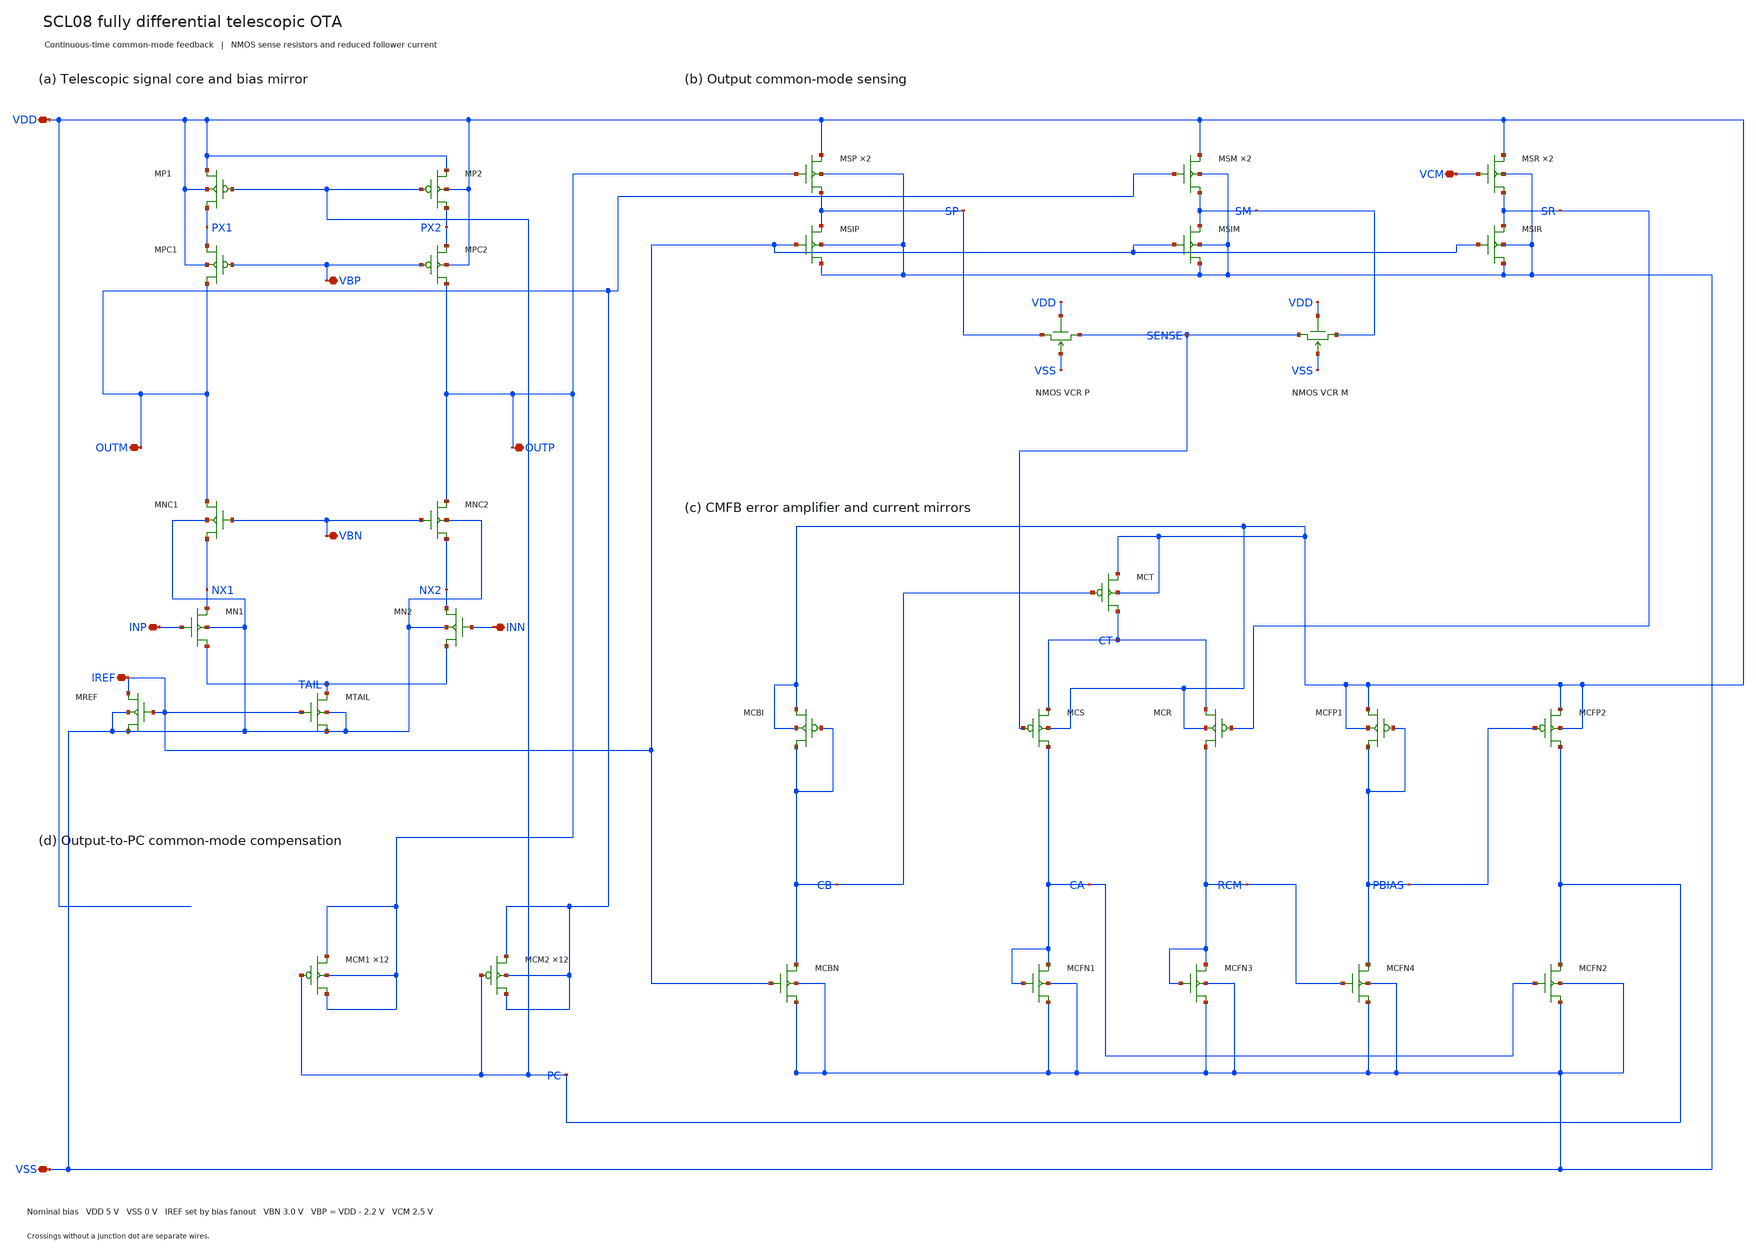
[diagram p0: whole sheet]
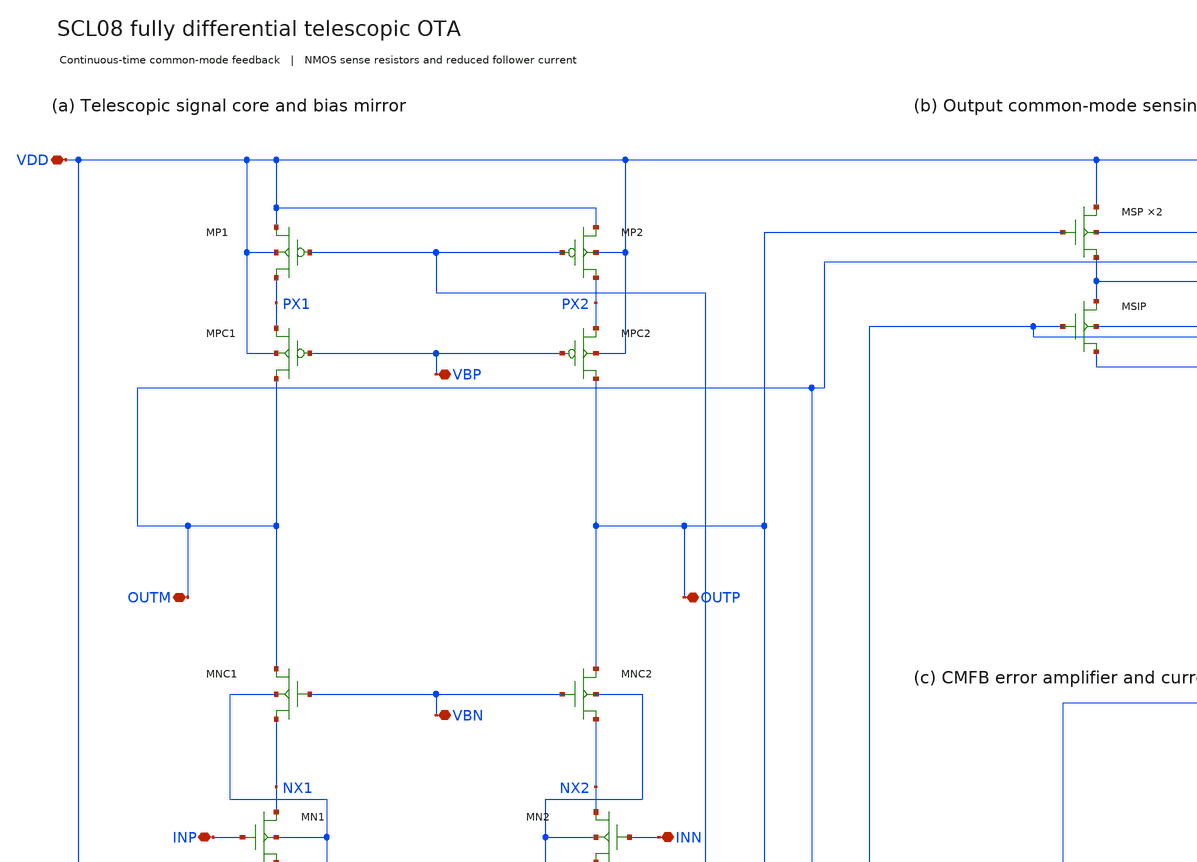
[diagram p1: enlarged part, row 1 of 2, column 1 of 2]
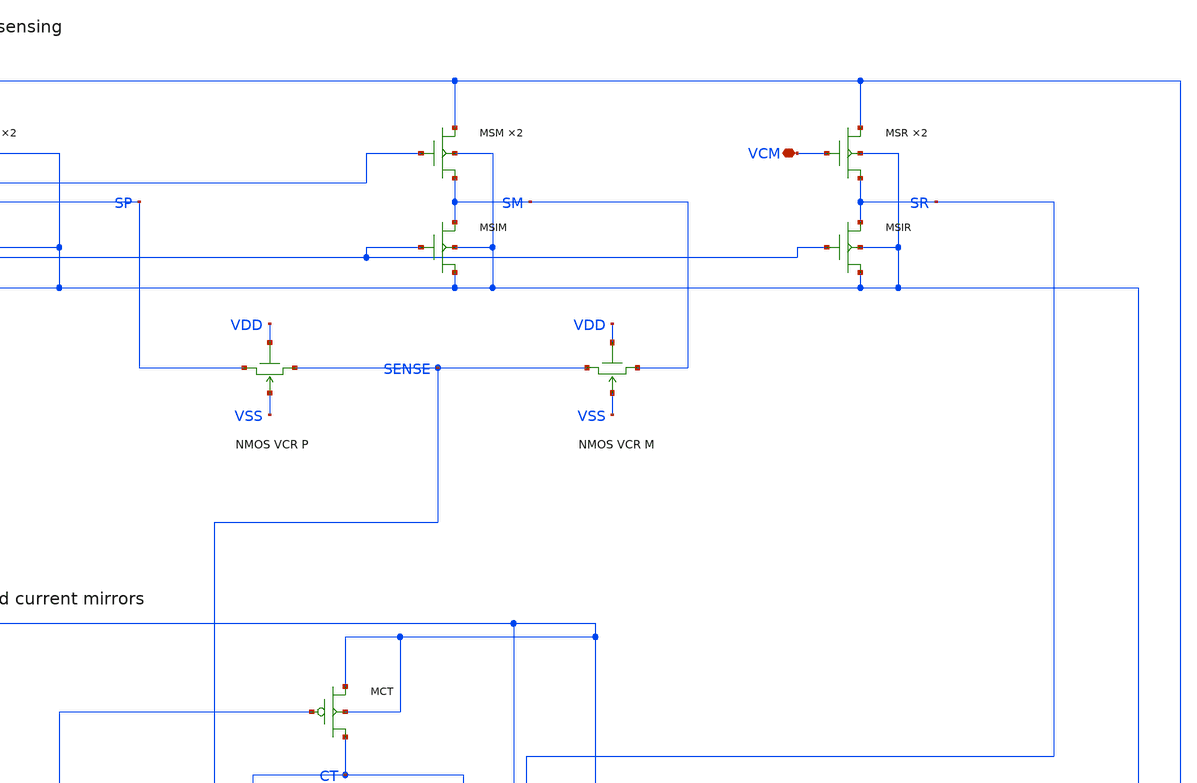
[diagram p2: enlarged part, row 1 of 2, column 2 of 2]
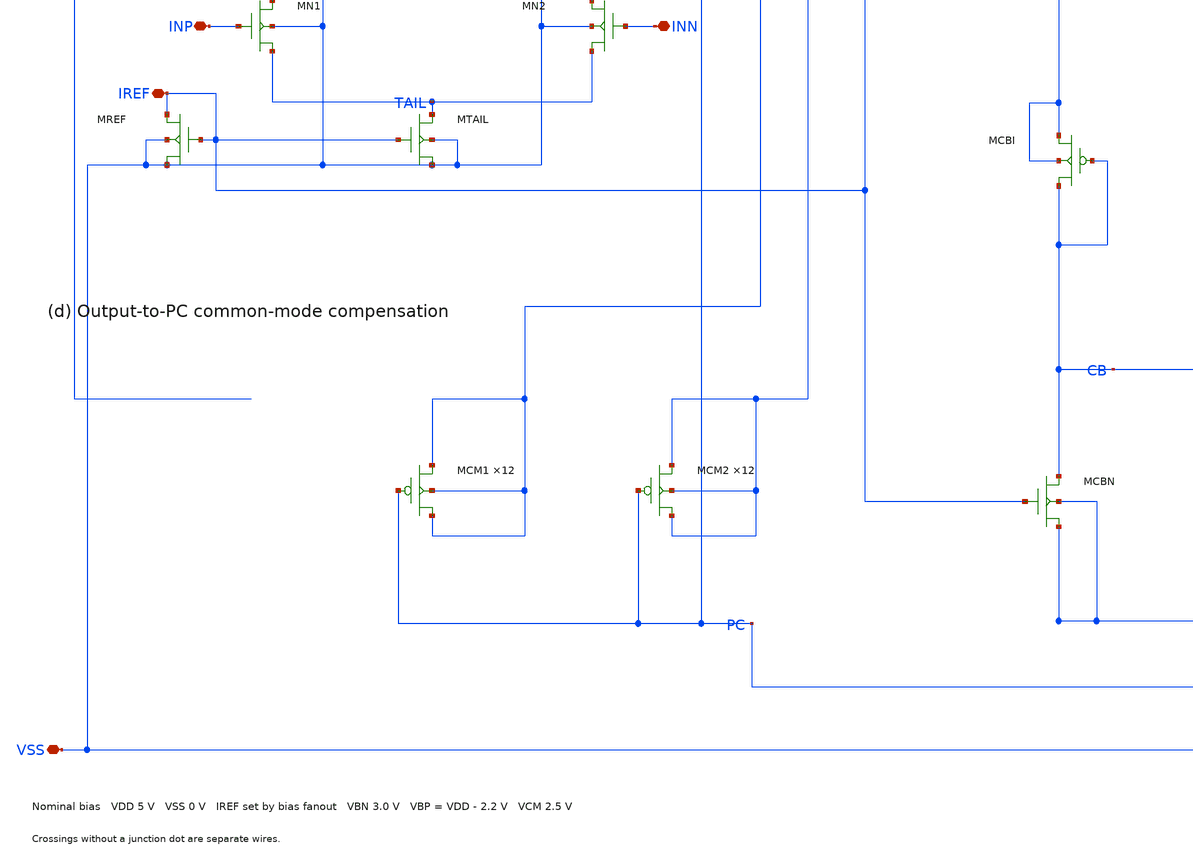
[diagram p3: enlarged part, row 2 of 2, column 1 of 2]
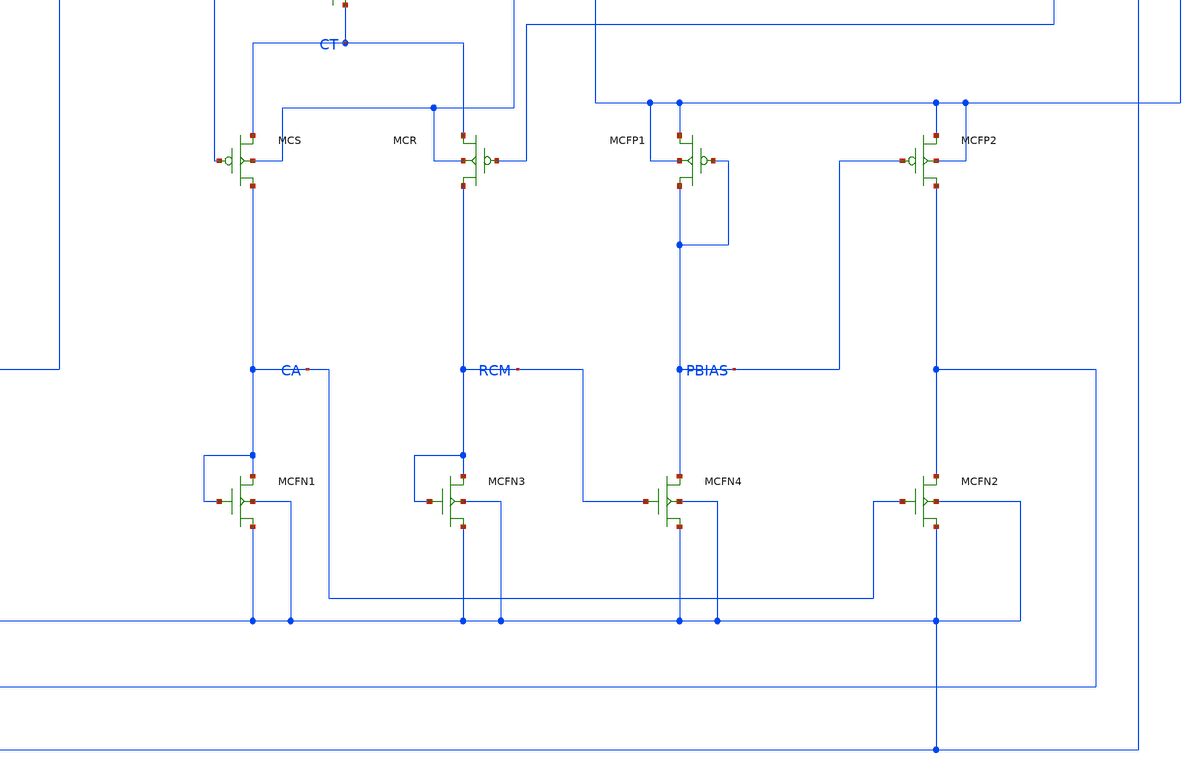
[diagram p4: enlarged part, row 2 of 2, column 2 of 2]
** sch_path: Mixed_Signal/Integrated_Design/schematic/ota_vcr_no_mcc.sch
**.subckt ota_vcr_no_mcc INP INN OUTP OUTM VDD VSS IREF VCM VBN VBP
*.iopin INP
*.iopin INN
*.iopin OUTP
*.iopin OUTM
*.iopin VDD
*.iopin VSS
*.iopin IREF
*.iopin VCM
*.iopin VBN
*.iopin VBP
MP1 PX1 PC VDD VDD P w=40u l=3.2u AD=180p AS=180p PD=89u PS=89u m=1
MPC1 OUTM VBP PX1 VDD P w=60u l=2.4u AD=270p AS=270p PD=129u PS=129u m=1
MNC1 OUTM VBN NX1 VSS N w=30u l=2.4u AD=135p AS=135p PD=69u PS=69u m=1
MN1 NX1 INP TAIL VSS N w=15u l=2.4u AD=67.5p AS=67.5p PD=39u PS=39u m=1
MP2 PX2 PC VDD VDD P w=40u l=3.2u AD=180p AS=180p PD=89u PS=89u m=1
MPC2 OUTP VBP PX2 VDD P w=60u l=2.4u AD=270p AS=270p PD=129u PS=129u m=1
MNC2 OUTP VBN NX2 VSS N w=30u l=2.4u AD=135p AS=135p PD=69u PS=69u m=1
MN2 NX2 INN TAIL VSS N w=15u l=2.4u AD=67.5p AS=67.5p PD=39u PS=39u m=1
MTAIL TAIL IREF VSS VSS N w=80.0u l=3.2u AD=360p AS=360p PD=169u PS=169u m=1
MREF IREF IREF VSS VSS N w=20u l=3.2u AD=90p AS=90p PD=49u PS=49u m=1
MSP VDD OUTP SP VSS N w=20u l=1.6u AD=90p AS=90p PD=49u PS=49u m=2
MSIP SP IREF VSS VSS N w=20u l=3.2u AD=90p AS=90p PD=49u PS=49u m=1
MSM VDD OUTM SM VSS N w=20u l=1.6u AD=90p AS=90p PD=49u PS=49u m=2
MSIM SM IREF VSS VSS N w=20u l=3.2u AD=90p AS=90p PD=49u PS=49u m=1
MSR VDD VCM SR VSS N w=20u l=1.6u AD=90p AS=90p PD=49u PS=49u m=2
MSIR SR IREF VSS VSS N w=20u l=3.2u AD=90p AS=90p PD=49u PS=49u m=1
MVCRPN SP VDD SENSE VSS N W=2.5u L=51.218u M=1 AD=11.25p AS=11.25p PD=14u PS=14u
MVCRMN SM VDD SENSE VSS N W=2.5u L=51.218u M=1 AD=11.25p AS=11.25p PD=14u PS=14u
MCT CT CB VDD VDD P w=10u l=3.2u AD=45p AS=45p PD=29u PS=29u m=1
MCBI CB CB VDD VDD P w=20u l=3.2u AD=90p AS=90p PD=49u PS=49u m=1
MCBN CB IREF VSS VSS N w=11.428571u l=3.2u AD=51.4286p AS=51.4286p PD=31.8571u PS=31.8571u m=1
MCS CA SENSE CT VDD P w=5u l=2.4u AD=22.5p AS=22.5p PD=19u PS=19u m=1
MCR RCM SR CT VDD P w=5u l=2.4u AD=22.5p AS=22.5p PD=19u PS=19u m=1
MCFN1 CA CA VSS VSS N w=10u l=3.2u AD=45p AS=45p PD=29u PS=29u m=1
MCFN3 RCM RCM VSS VSS N w=10u l=3.2u AD=45p AS=45p PD=29u PS=29u m=1
MCFP1 PBIAS PBIAS VDD VDD P w=10u l=3.2u AD=45p AS=45p PD=29u PS=29u m=1
MCFN4 PBIAS RCM VSS VSS N w=10u l=3.2u AD=45p AS=45p PD=29u PS=29u m=1
MCFP2 PC PBIAS VDD VDD P w=10u l=3.2u AD=45p AS=45p PD=29u PS=29u m=1
MCFN2 PC CA VSS VSS N w=10u l=3.2u AD=45p AS=45p PD=29u PS=29u m=1
MCM1 OUTP PC OUTP OUTP P w=20u l=10u AD=90p AS=90p PD=49u PS=49u m=12
MCM2 OUTM PC OUTM OUTM P w=20u l=10u AD=90p AS=90p PD=49u PS=49u m=12
**.ends
.end
